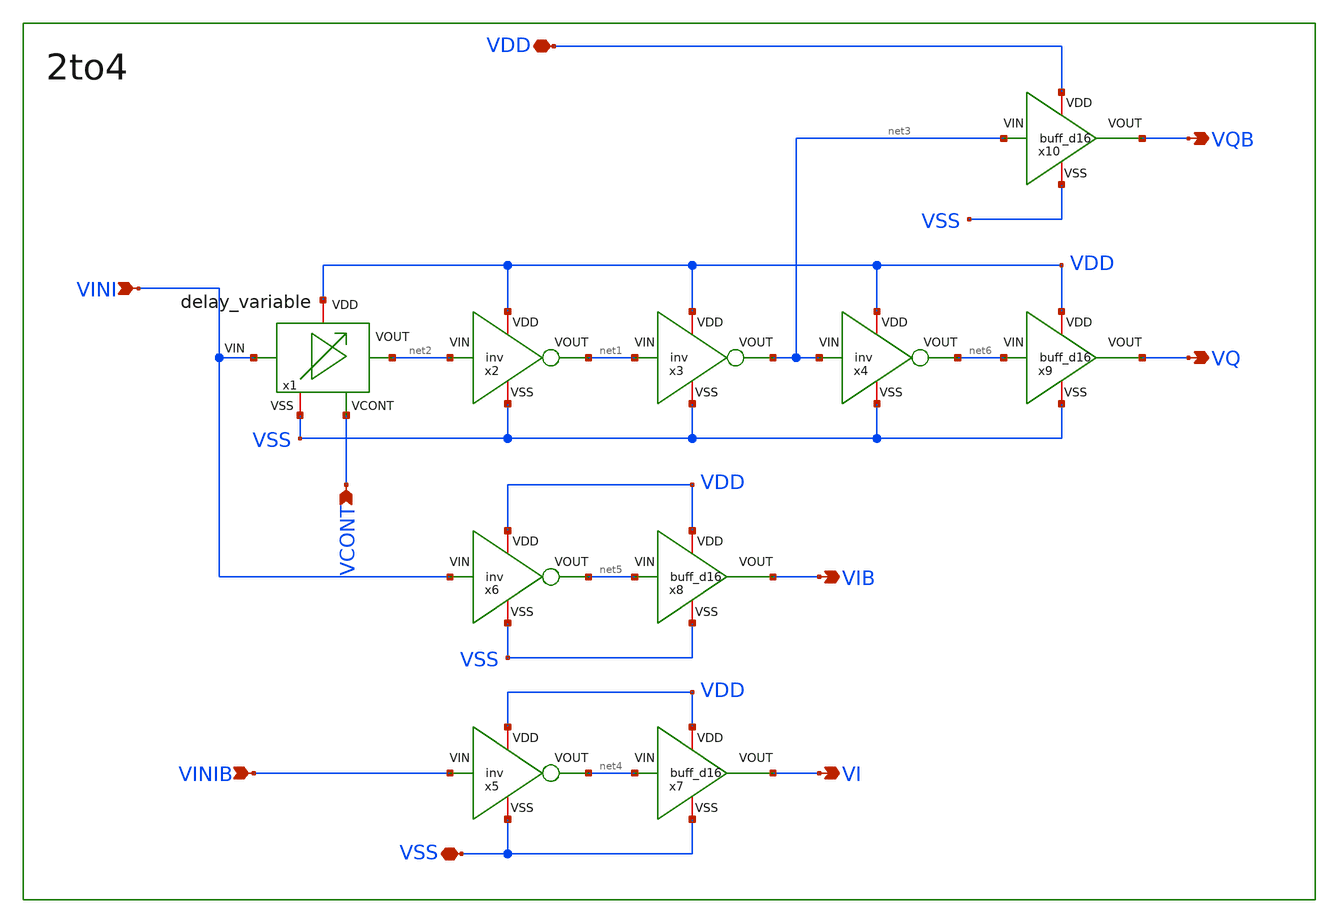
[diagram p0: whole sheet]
** sch_path: 2to4/2to4prelim.sch
**.subckt 2to4prelim VDD VSS VCONT VINI VIB VQ VQB VINIB VI
*.iopin VDD
*.iopin VSS
*.ipin VCONT
*.ipin VINI
*.opin VIB
*.opin VQ
*.opin VQB
*.ipin VINIB
*.opin VI
x1 VDD VINI net2 VCONT VSS delay_variable
x2 VDD net1 net2 VSS inv
x3 VDD net3 net1 VSS inv
x4 VDD net6 net3 VSS inv
x6 VDD net5 VINI VSS inv
x5 VDD net4 VINIB VSS inv
x7 VDD VI net4 VSS buff_d16
x8 VDD VIB net5 VSS buff_d16
x9 VDD VQ net6 VSS buff_d16
x10 VDD VQB net3 VSS buff_d16
**.ends
.end
